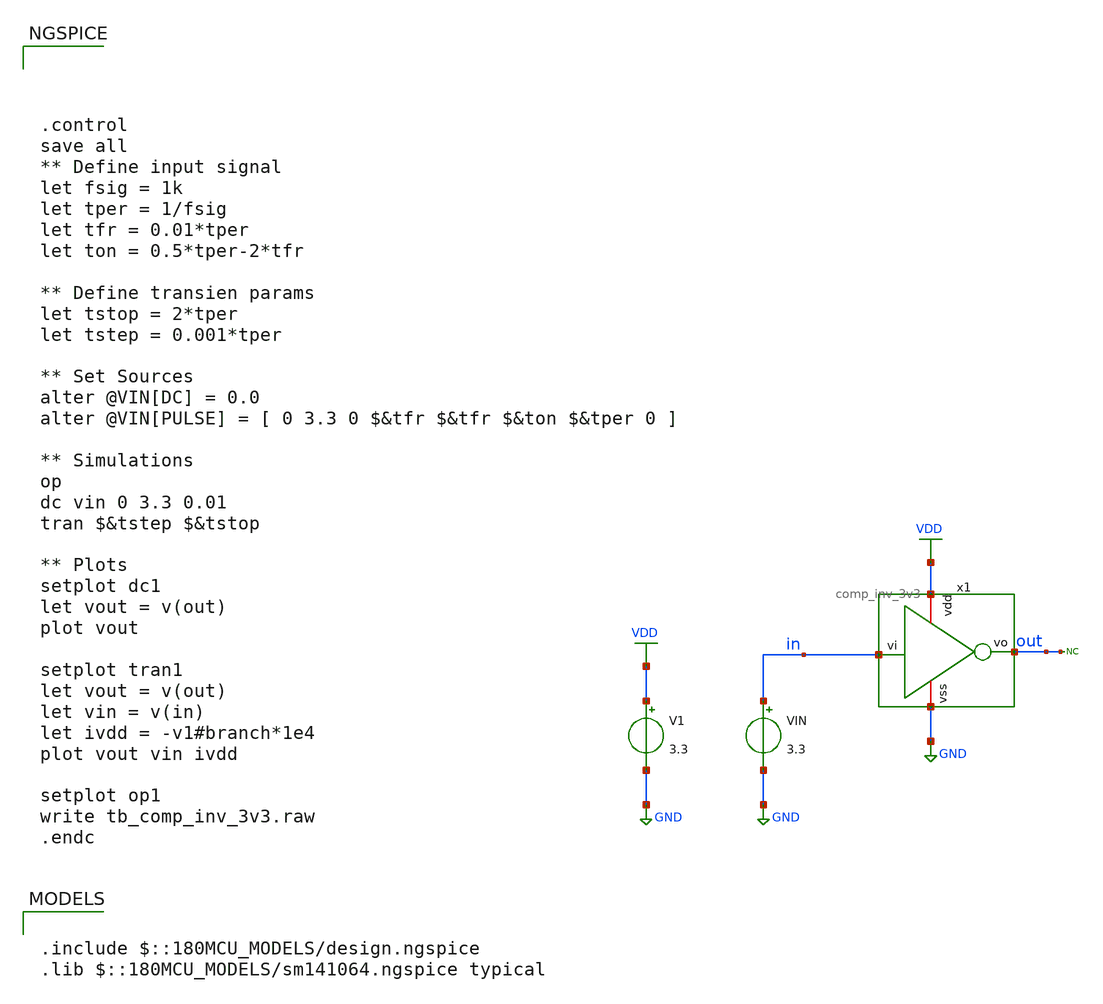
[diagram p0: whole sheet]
** sch_path: xschem/sar_adc/blocks/comparator/testbench/tb_comp_inv_3v3.sch
**.subckt tb_comp_inv_3v3
V1 VDD GND 3.3
VIN in GND 3.3
* noconn out
x1 VDD in out GND comp_inv_3v3
**** begin user architecture code

.include $::180MCU_MODELS/design.ngspice
.lib $::180MCU_MODELS/sm141064.ngspice typical





.control
save all
** Define input signal
let fsig = 1k
let tper = 1/fsig
let tfr = 0.01*tper
let ton = 0.5*tper-2*tfr

** Define transien params
let tstop = 2*tper
let tstep = 0.001*tper

** Set Sources
alter @VIN[DC] = 0.0
alter @VIN[PULSE] = [ 0 3.3 0 $&tfr $&tfr $&ton $&tper 0 ]

** Simulations
op
dc vin 0 3.3 0.01
tran $&tstep $&tstop

** Plots
setplot dc1
let vout = v(out)
plot vout

setplot tran1
let vout = v(out)
let vin = v(in)
let ivdd = -v1#branch*1e4
plot vout vin ivdd

setplot op1
write tb_comp_inv_3v3.raw
.endc


**** end user architecture code
**.ends

* expanding   symbol:  sar_adc/blocks/comparator/comp_inv_3v3.sym # of pins=4
** sym_path: xschem/sar_adc/blocks/comparator/comp_inv_3v3.sym
** sch_path: xschem/sar_adc/blocks/comparator/comp_inv_3v3.sch
.subckt comp_inv_3v3 vdd vi vo vss
*.ipin vi
*.opin vo
*.iopin vdd
*.iopin vss
XM2 vo vi vdd vdd pfet_03v3 L=0.28u W=0.80u nf=1 ad='int((nf+1)/2) * W/nf * 0.18u' as='int((nf+2)/2) * W/nf * 0.18u'
+ pd='2*int((nf+1)/2) * (W/nf + 0.18u)' ps='2*int((nf+2)/2) * (W/nf + 0.18u)' nrd='0.18u / W' nrs='0.18u / W'
+ sa=0 sb=0 sd=0 m=1
XM1 vo vi vss vss nfet_03v3 L=0.28u W=0.42u nf=1 ad='int((nf+1)/2) * W/nf * 0.18u' as='int((nf+2)/2) * W/nf * 0.18u'
+ pd='2*int((nf+1)/2) * (W/nf + 0.18u)' ps='2*int((nf+2)/2) * (W/nf + 0.18u)' nrd='0.18u / W' nrs='0.18u / W'
+ sa=0 sb=0 sd=0 m=1
.ends

.GLOBAL VDD
.GLOBAL GND
.end
